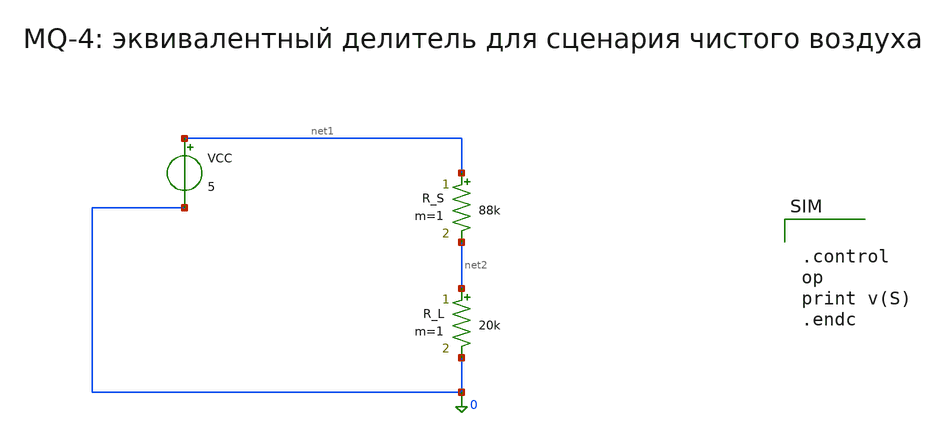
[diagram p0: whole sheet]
** sch_path: docs/figures/xschem_probe/mq4_divider.sch
**.subckt mq4_divider
VCC net1 0 5
R_S net1 net2 88k m=1
R_L net2 0 20k m=1
**** begin user architecture code


.control
op
print v(S)
.endc

**** end user architecture code
**.ends
.end
